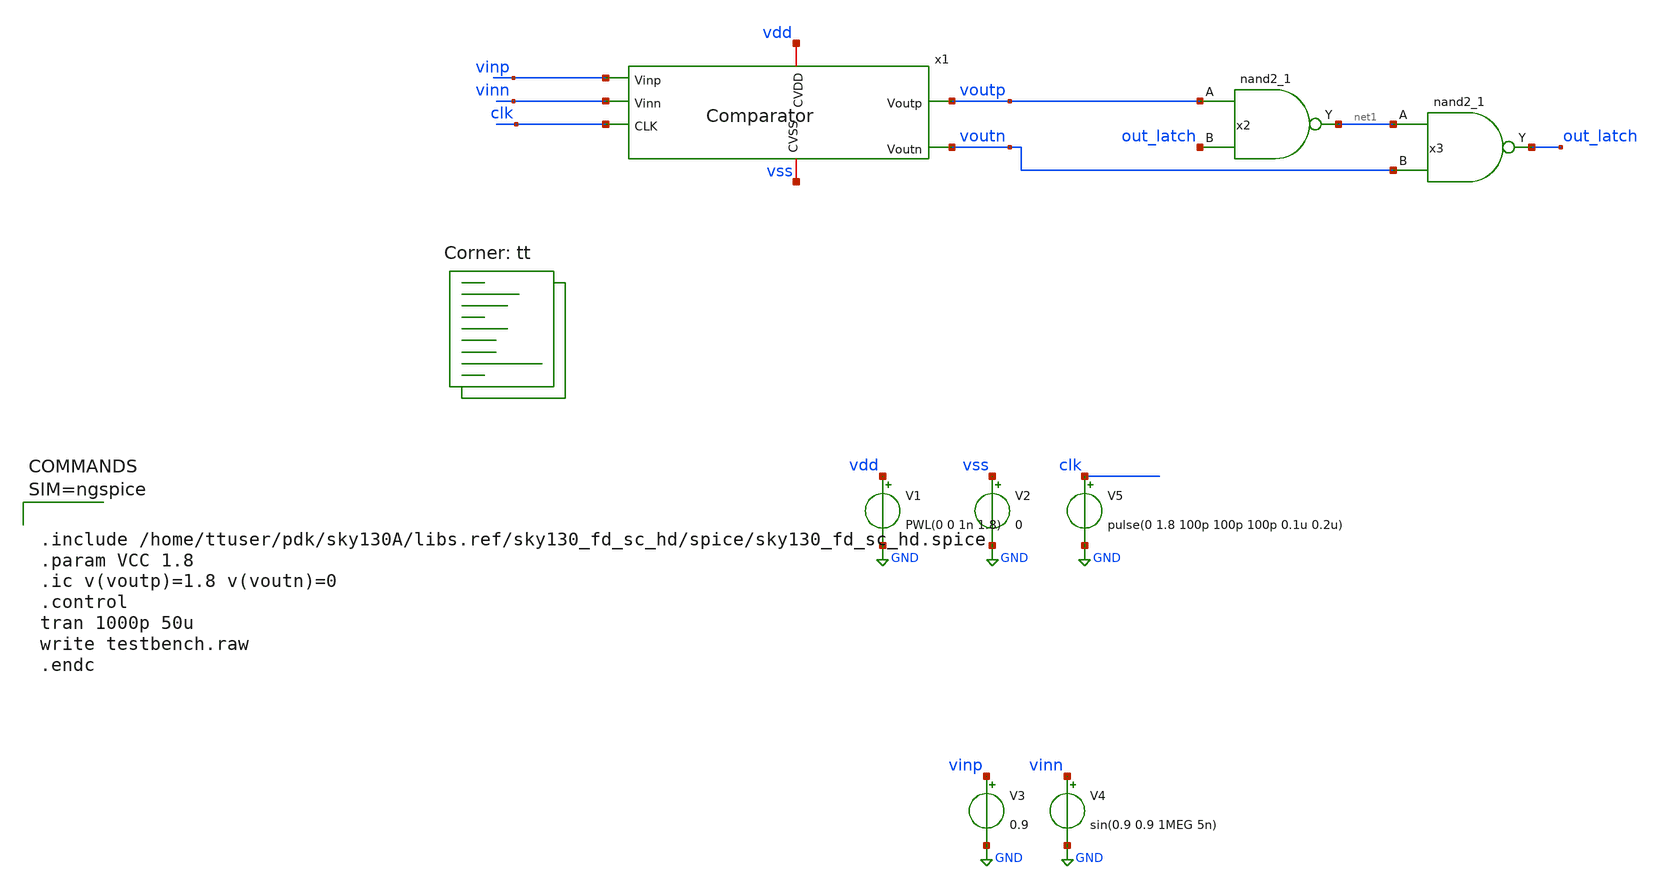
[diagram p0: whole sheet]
** sch_path: xschem/Comparator_tb.sch
**.subckt Comparator_tb
V1 vdd GND PWL(0 0 1n 1.8)
V2 vss GND 0
V3 vinp GND 0.9
V4 vinn GND sin(0.9 0.9 1MEG 5n)
x1 vinp vinn vdd clk voutp vss voutn Comparator
V5 clk GND pulse(0 1.8 100p 100p 100p 0.1u 0.2u)
x2 voutp out_latch vss vss vdd vdd net1 sky130_fd_sc_hd__nand2_1
x3 net1 voutn vss vss vdd vdd out_latch sky130_fd_sc_hd__nand2_1
**** begin user architecture code



.include /home/ttuser/pdk/sky130A/libs.ref/sky130_fd_sc_hd/spice/sky130_fd_sc_hd.spice
.param VCC 1.8
.ic v(voutp)=1.8 v(voutn)=0
.control
tran 1000p 50u
write testbench.raw
.endc



.lib $::SKYWATER_MODELS/sky130.lib.spice tt
**** end user architecture code
**.ends

* expanding   symbol:  Comparator.sym # of pins=7
** sym_path: xschem/Comparator.sym
** sch_path: xschem/Comparator.sch
.subckt Comparator Vinp Vinn CVDD CLK Voutp CVSS Voutn
*.iopin CVDD
*.iopin CVSS
*.ipin Vinp
*.ipin Vinn
*.ipin CLK
*.opin Voutp
*.opin Voutn
XM1 Voutn Voutp CVDD CVDD sky130_fd_pr__pfet_01v8 L=0.15 W=10 nf=2 ad='int((nf+1)/2) * W/nf * 0.29' as='int((nf+2)/2) * W/nf * 0.29'
+ pd='2*int((nf+1)/2) * (W/nf + 0.29)' ps='2*int((nf+2)/2) * (W/nf + 0.29)' nrd='0.29 / W' nrs='0.29 / W'
+ sa=0 sb=0 sd=0 mult=8 m=8
XM2 net2 Vinp net3 CVSS sky130_fd_pr__nfet_01v8 L=0.15 W=10 nf=2 ad='int((nf+1)/2) * W/nf * 0.29' as='int((nf+2)/2) * W/nf * 0.29'
+ pd='2*int((nf+1)/2) * (W/nf + 0.29)' ps='2*int((nf+2)/2) * (W/nf + 0.29)' nrd='0.29 / W' nrs='0.29 / W'
+ sa=0 sb=0 sd=0 mult=4 m=4
XM3 net1 Vinn net3 CVSS sky130_fd_pr__nfet_01v8 L=0.15 W=10 nf=2 ad='int((nf+1)/2) * W/nf * 0.29' as='int((nf+2)/2) * W/nf * 0.29'
+ pd='2*int((nf+1)/2) * (W/nf + 0.29)' ps='2*int((nf+2)/2) * (W/nf + 0.29)' nrd='0.29 / W' nrs='0.29 / W'
+ sa=0 sb=0 sd=0 mult=4 m=4
XM4 net3 CLK CVSS CVSS sky130_fd_pr__nfet_01v8 L=0.15 W=10 nf=2 ad='int((nf+1)/2) * W/nf * 0.29' as='int((nf+2)/2) * W/nf * 0.29'
+ pd='2*int((nf+1)/2) * (W/nf + 0.29)' ps='2*int((nf+2)/2) * (W/nf + 0.29)' nrd='0.29 / W' nrs='0.29 / W'
+ sa=0 sb=0 sd=0 mult=1 m=1
XM5 Voutn Voutp net1 CVSS sky130_fd_pr__nfet_01v8 L=0.15 W=10 nf=2 ad='int((nf+1)/2) * W/nf * 0.29' as='int((nf+2)/2) * W/nf * 0.29'
+ pd='2*int((nf+1)/2) * (W/nf + 0.29)' ps='2*int((nf+2)/2) * (W/nf + 0.29)' nrd='0.29 / W' nrs='0.29 / W'
+ sa=0 sb=0 sd=0 mult=4 m=4
XM6 Voutp Voutn net2 CVSS sky130_fd_pr__nfet_01v8 L=0.15 W=10 nf=2 ad='int((nf+1)/2) * W/nf * 0.29' as='int((nf+2)/2) * W/nf * 0.29'
+ pd='2*int((nf+1)/2) * (W/nf + 0.29)' ps='2*int((nf+2)/2) * (W/nf + 0.29)' nrd='0.29 / W' nrs='0.29 / W'
+ sa=0 sb=0 sd=0 mult=4 m=4
XM7 Voutp Voutn CVDD CVDD sky130_fd_pr__pfet_01v8 L=0.15 W=10 nf=2 ad='int((nf+1)/2) * W/nf * 0.29' as='int((nf+2)/2) * W/nf * 0.29'
+ pd='2*int((nf+1)/2) * (W/nf + 0.29)' ps='2*int((nf+2)/2) * (W/nf + 0.29)' nrd='0.29 / W' nrs='0.29 / W'
+ sa=0 sb=0 sd=0 mult=8 m=8
XM8 Voutp CLK CVDD CVDD sky130_fd_pr__pfet_01v8 L=0.15 W=10 nf=1 ad='int((nf+1)/2) * W/nf * 0.29' as='int((nf+2)/2) * W/nf * 0.29'
+ pd='2*int((nf+1)/2) * (W/nf + 0.29)' ps='2*int((nf+2)/2) * (W/nf + 0.29)' nrd='0.29 / W' nrs='0.29 / W'
+ sa=0 sb=0 sd=0 mult=1 m=1
XM9 net2 CLK CVDD CVDD sky130_fd_pr__pfet_01v8 L=0.15 W=10 nf=1 ad='int((nf+1)/2) * W/nf * 0.29' as='int((nf+2)/2) * W/nf * 0.29'
+ pd='2*int((nf+1)/2) * (W/nf + 0.29)' ps='2*int((nf+2)/2) * (W/nf + 0.29)' nrd='0.29 / W' nrs='0.29 / W'
+ sa=0 sb=0 sd=0 mult=1 m=1
XM10 Voutn CLK CVDD CVDD sky130_fd_pr__pfet_01v8 L=0.15 W=10 nf=1 ad='int((nf+1)/2) * W/nf * 0.29' as='int((nf+2)/2) * W/nf * 0.29'
+ pd='2*int((nf+1)/2) * (W/nf + 0.29)' ps='2*int((nf+2)/2) * (W/nf + 0.29)' nrd='0.29 / W' nrs='0.29 / W'
+ sa=0 sb=0 sd=0 mult=1 m=1
XM11 net1 CLK CVDD CVDD sky130_fd_pr__pfet_01v8 L=0.15 W=10 nf=1 ad='int((nf+1)/2) * W/nf * 0.29' as='int((nf+2)/2) * W/nf * 0.29'
+ pd='2*int((nf+1)/2) * (W/nf + 0.29)' ps='2*int((nf+2)/2) * (W/nf + 0.29)' nrd='0.29 / W' nrs='0.29 / W'
+ sa=0 sb=0 sd=0 mult=1 m=1
.ends

.GLOBAL GND
.end
